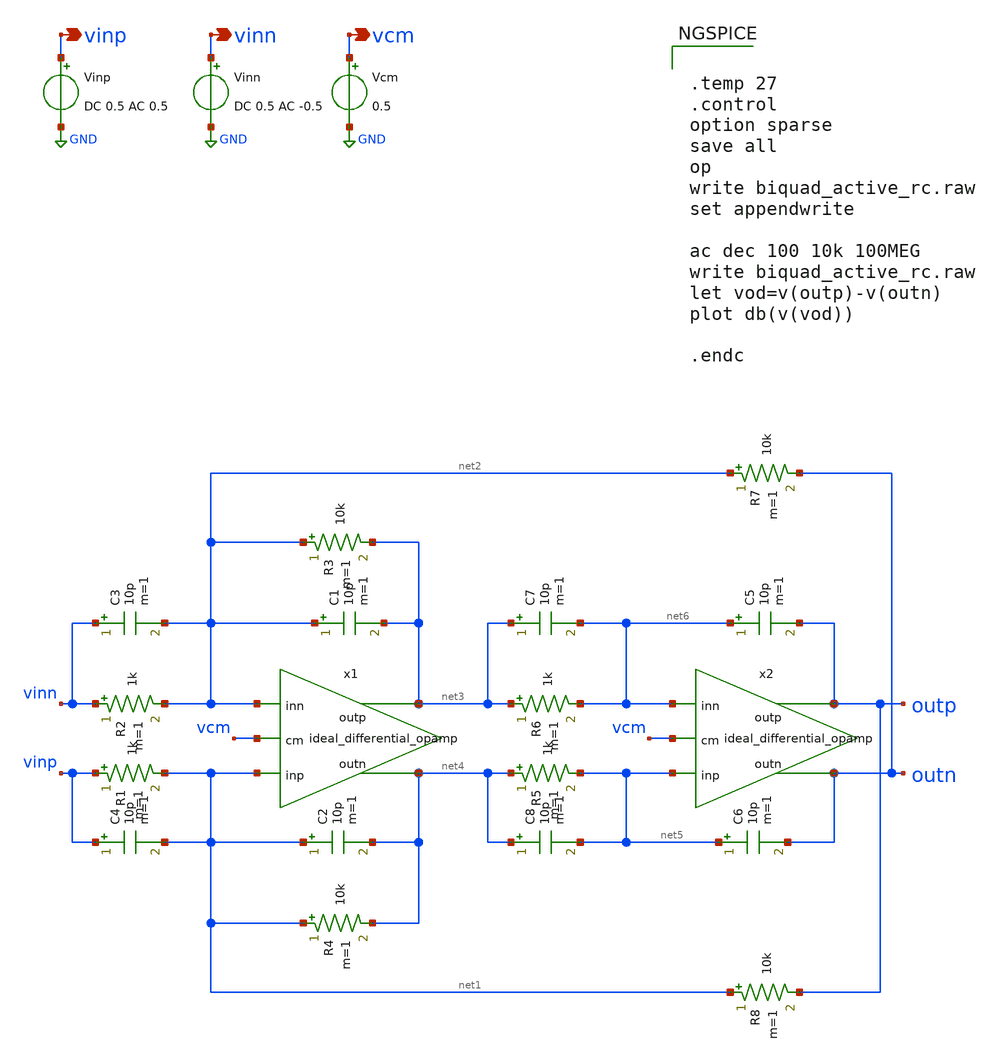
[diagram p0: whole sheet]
** sch_path: prj/template/2_Idealized_circuits/biquad_active_rc.sch
**.subckt biquad_active_rc vinp vinn vcm
*.opin vinp
*.opin vinn
*.opin vcm
C1 net2 net3 10p m=1
Vinp vinp GND DC 0.5 AC 0.5
Vinn vinn GND DC 0.5 AC -0.5
Vcm vcm GND 0.5
x1 net1 net2 net3 net4 vcm ideal_differential_opamp
R1 vinp net1 1k m=1
R2 vinn net2 1k m=1
R3 net2 net3 10k m=1
R4 net1 net4 10k m=1
C2 net1 net4 10p m=1
C3 vinn net2 10p m=1
C4 vinp net1 10p m=1
C5 net6 outp 10p m=1
x2 net5 net6 outp outn vcm ideal_differential_opamp
R5 net4 net5 1k m=1
R6 net3 net6 1k m=1
R7 net2 outn 10k m=1
R8 net1 outp 10k m=1
C6 net5 outn 10p m=1
C7 net3 net6 10p m=1
C8 net4 net5 10p m=1
**** begin user architecture code


.temp 27
.control
option sparse
save all
op
write biquad_active_rc.raw
set appendwrite

ac dec 100 10k 100MEG
write biquad_active_rc.raw
let vod=v(outp)-v(outn)
plot db(v(vod))

.endc


**** end user architecture code
**.ends

* expanding   symbol:  ideal_differential_opamp.sym # of pins=5
** sym_path: prj/template/2_Idealized_circuits/ideal_differential_opamp.sym
** sch_path: prj/template/2_Idealized_circuits/ideal_differential_opamp.sch
.subckt ideal_differential_opamp inp inn outp outn cm
*.opin outp
*.ipin inp
*.ipin inn
*.opin outn
*.ipin cm
G1 outp net1 inp inn 100Meg
R1 outp net1 1 m=1
G2 net1 outn inp inn 100Meg
R2 net1 outn 1 m=1
G3 net1 GND cm net1 100Meg
.ends

.GLOBAL GND
.end
